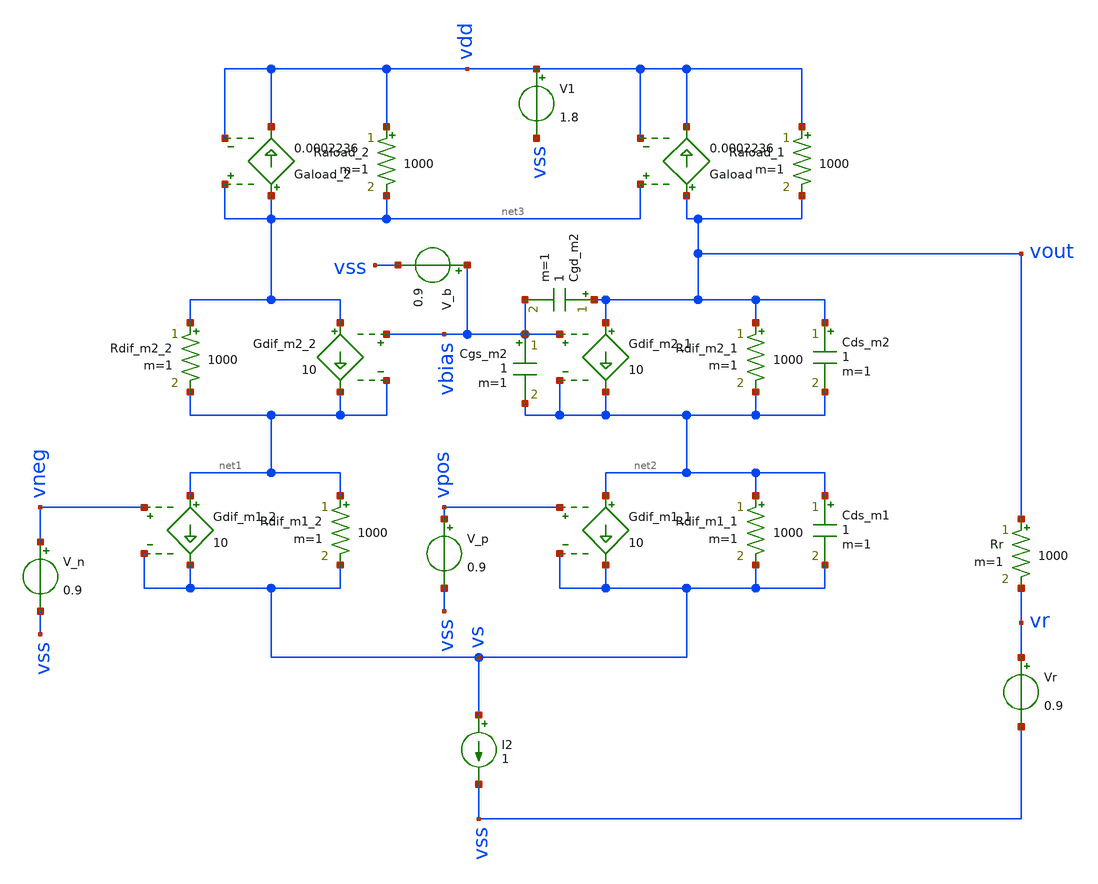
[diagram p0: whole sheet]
** sch_path: test/sstadex/xschem/ota_cc_cap_r.sch
**.subckt ota_cc_cap_r
Rdif_m1_2 net1 vs 1000 m=1
Gdif_m1_2 net1 vs vneg vs 10
Rdif_m1_1 net2 vs 1000 m=1
Gdif_m1_1 net2 vs vpos vs 10
I2 vs vss 1
V1 vdd vss 1.8
V_n vneg vss 0.9
V_p vpos vss 0.9
Raload_1 vdd vout 1000 m=1
Raload_2 vdd net3 1000 m=1
Gaload vout vdd net3 vdd 0.0002236
Gaload_2 net3 vdd net3 vdd 0.0002236
Rdif_m2_1 vout net2 1000 m=1
Gdif_m2_1 vout net2 vbias net2 10
Rdif_m2_2 net3 net1 1000 m=1
Gdif_m2_2 net3 net1 vbias net1 10
V_b vbias vss 0.9
Cds_m1 net2 vs 1 m=1
Cds_m2 vout net2 1 m=1
Cgs_m2 vbias net2 1 m=1
Cgd_m2 vout vbias 1 m=1
Vr vr vss 0.9
Rr vout vr 1000 m=1
**.ends
.end
